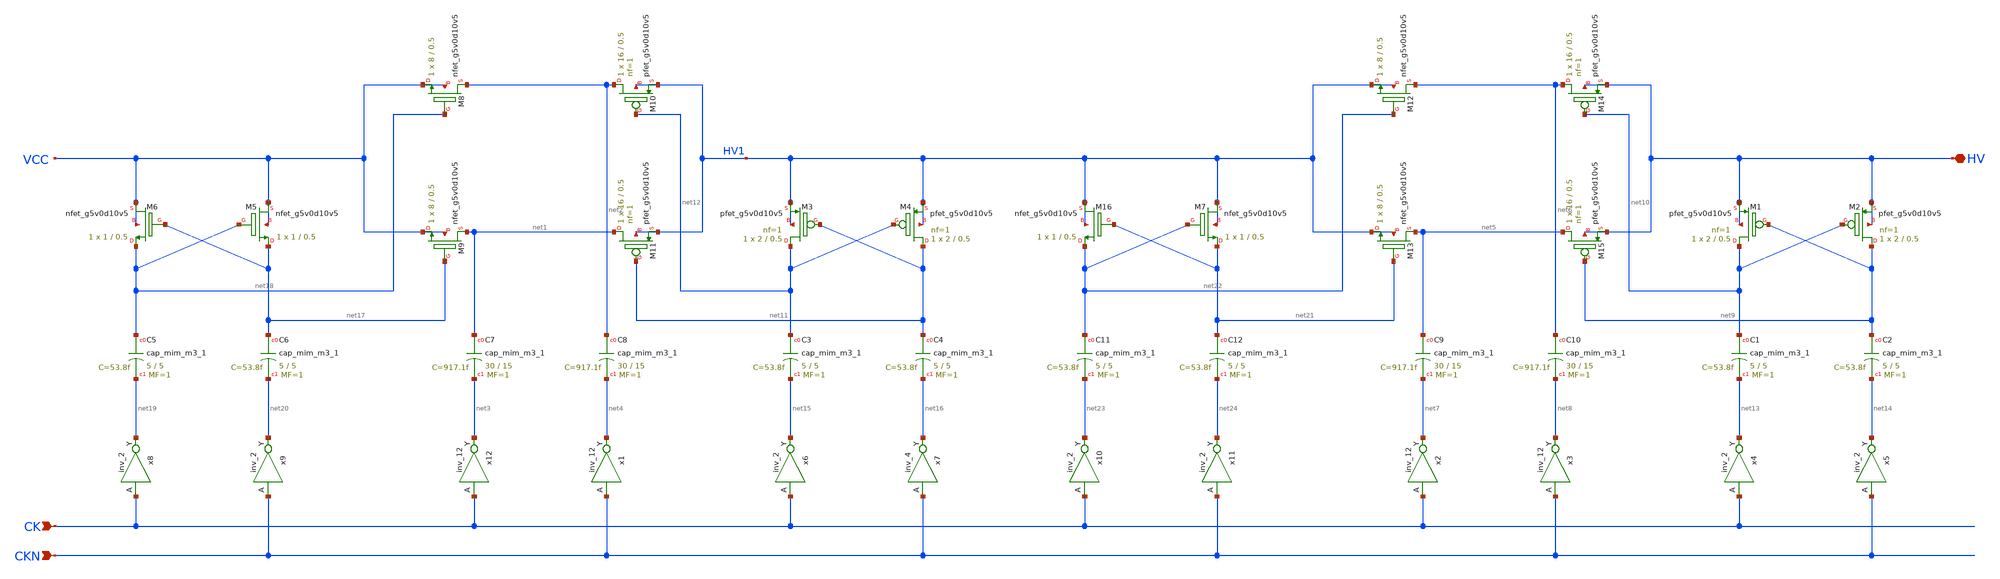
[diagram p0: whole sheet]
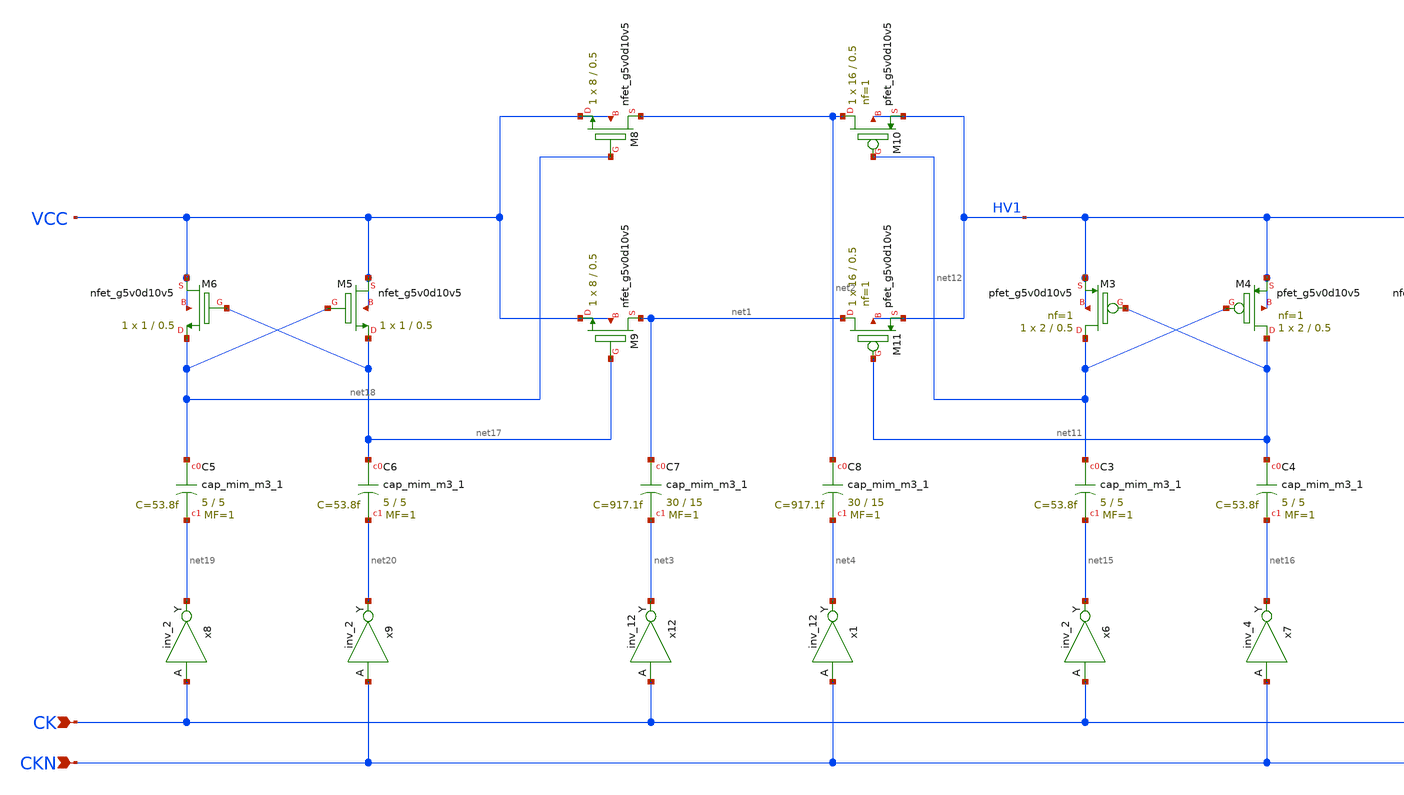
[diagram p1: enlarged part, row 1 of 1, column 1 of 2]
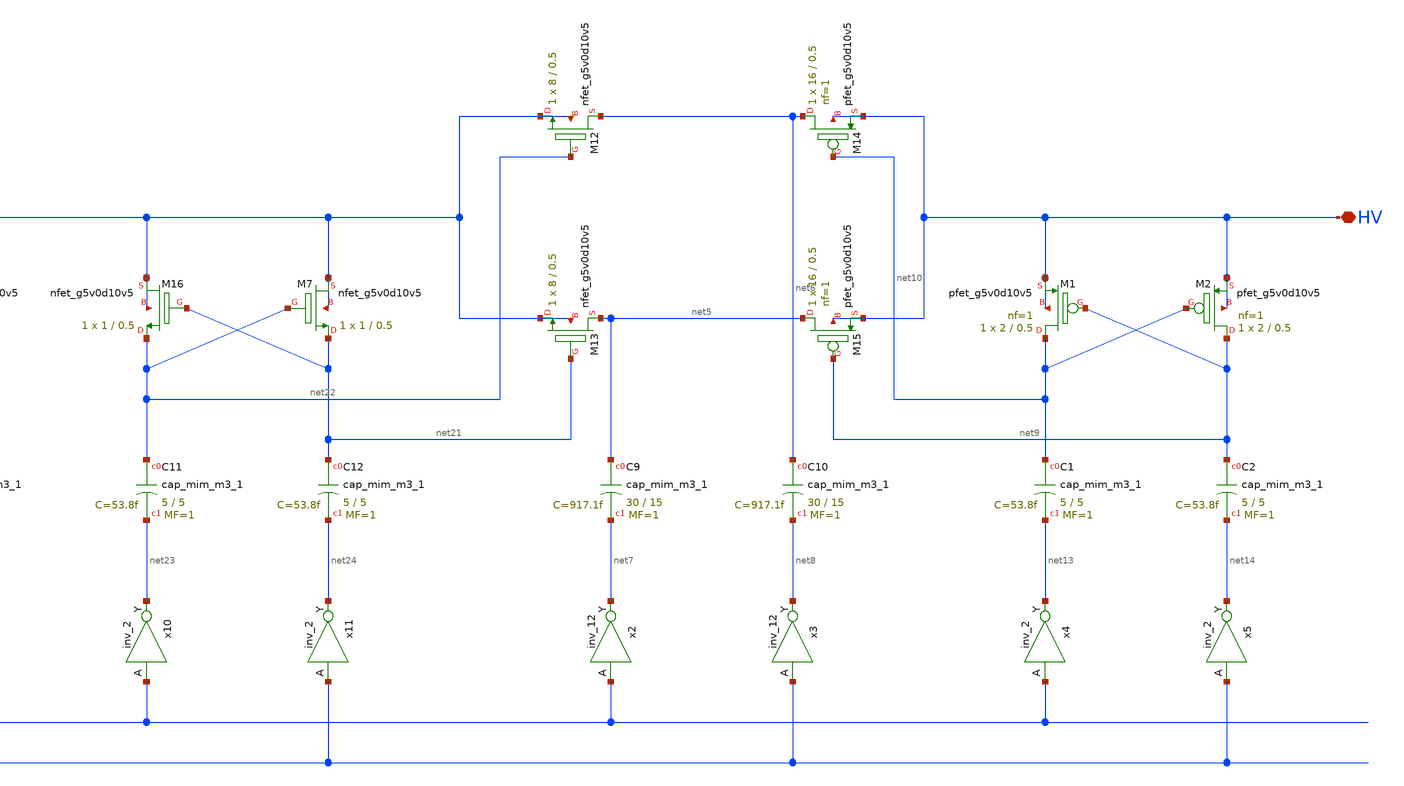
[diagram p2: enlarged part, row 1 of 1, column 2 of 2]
** sch_path: sky130_tests/charge_pump2.sch
**.subckt charge_pump2 HV CK CKN
*.iopin HV
*.ipin CK
*.ipin CKN
XM8 net2 net18 VCC VCC sky130_fd_pr__nfet_g5v0d10v5 W=8 L=0.5 ad='int((nf+1)/2) * W/nf * 0.29' pd='2*int((nf+1)/2) * (W/nf + 0.29)'
+ as='int((nf+2)/2) * W/nf * 0.29' ps='2*int((nf+2)/2) * (W/nf + 0.29)' nrd='0.29 / W' nrs='0.29 / W' sa=0
+ sb=0 sd=0 nf=1 mult=1
XM9 net1 net17 VCC VCC sky130_fd_pr__nfet_g5v0d10v5 W=8 L=0.5 ad='int((nf+1)/2) * W/nf * 0.29' pd='2*int((nf+1)/2) * (W/nf + 0.29)'
+ as='int((nf+2)/2) * W/nf * 0.29' ps='2*int((nf+2)/2) * (W/nf + 0.29)' nrd='0.29 / W' nrs='0.29 / W' sa=0
+ sb=0 sd=0 nf=1 mult=1
XM10 net2 net12 HV1 HV1 sky130_fd_pr__pfet_g5v0d10v5 L=0.5 W=16 nf=1 ad='int((nf+1)/2) * W/nf * 0.29'
+ as='int((nf+2)/2) * W/nf * 0.29' pd='2*int((nf+1)/2) * (W/nf + 0.29)' ps='2*int((nf+2)/2) * (W/nf + 0.29)'
+ nrd='0.29 / W' nrs='0.29 / W' sa=0 sb=0 sd=0 mult=1 m=1
XM11 net1 net11 HV1 HV1 sky130_fd_pr__pfet_g5v0d10v5 L=0.5 W=16 nf=1 ad='int((nf+1)/2) * W/nf * 0.29'
+ as='int((nf+2)/2) * W/nf * 0.29' pd='2*int((nf+1)/2) * (W/nf + 0.29)' ps='2*int((nf+2)/2) * (W/nf + 0.29)'
+ nrd='0.29 / W' nrs='0.29 / W' sa=0 sb=0 sd=0 mult=1 m=1
XC7 net1 net3 sky130_fd_pr__cap_mim_m3_1 W=30 L=15 MF=1 m=1
XC8 net2 net4 sky130_fd_pr__cap_mim_m3_1 W=30 L=15 MF=1 m=1
XM12 net6 net22 HV1 HV1 sky130_fd_pr__nfet_g5v0d10v5 W=8 L=0.5 ad='int((nf+1)/2) * W/nf * 0.29' pd='2*int((nf+1)/2) * (W/nf + 0.29)'
+ as='int((nf+2)/2) * W/nf * 0.29' ps='2*int((nf+2)/2) * (W/nf + 0.29)' nrd='0.29 / W' nrs='0.29 / W' sa=0
+ sb=0 sd=0 nf=1 mult=1
XM13 net5 net21 HV1 HV1 sky130_fd_pr__nfet_g5v0d10v5 W=8 L=0.5 ad='int((nf+1)/2) * W/nf * 0.29' pd='2*int((nf+1)/2) * (W/nf + 0.29)'
+ as='int((nf+2)/2) * W/nf * 0.29' ps='2*int((nf+2)/2) * (W/nf + 0.29)' nrd='0.29 / W' nrs='0.29 / W' sa=0
+ sb=0 sd=0 nf=1 mult=1
XM14 net6 net10 HV HV sky130_fd_pr__pfet_g5v0d10v5 L=0.5 W=16 nf=1 ad='int((nf+1)/2) * W/nf * 0.29' as='int((nf+2)/2) * W/nf * 0.29'
+ pd='2*int((nf+1)/2) * (W/nf + 0.29)' ps='2*int((nf+2)/2) * (W/nf + 0.29)' nrd='0.29 / W' nrs='0.29 / W'
+ sa=0 sb=0 sd=0 mult=1 m=1
XM15 net5 net9 HV HV sky130_fd_pr__pfet_g5v0d10v5 L=0.5 W=16 nf=1 ad='int((nf+1)/2) * W/nf * 0.29' as='int((nf+2)/2) * W/nf * 0.29'
+ pd='2*int((nf+1)/2) * (W/nf + 0.29)' ps='2*int((nf+2)/2) * (W/nf + 0.29)' nrd='0.29 / W' nrs='0.29 / W'
+ sa=0 sb=0 sd=0 mult=1 m=1
XC9 net5 net7 sky130_fd_pr__cap_mim_m3_1 W=30 L=15 MF=1 m=1
XC10 net6 net8 sky130_fd_pr__cap_mim_m3_1 W=30 L=15 MF=1 m=1
x12 CK GND GND VCC VCC net3 sky130_fd_sc_hd__inv_12
x1 CKN GND GND VCC VCC net4 sky130_fd_sc_hd__inv_12
x2 CK GND GND VCC VCC net7 sky130_fd_sc_hd__inv_12
x3 CKN GND GND VCC VCC net8 sky130_fd_sc_hd__inv_12
XM1 net10 net9 HV HV sky130_fd_pr__pfet_g5v0d10v5 L=0.5 W=2 nf=1 ad='int((nf+1)/2) * W/nf * 0.29' as='int((nf+2)/2) * W/nf * 0.29'
+ pd='2*int((nf+1)/2) * (W/nf + 0.29)' ps='2*int((nf+2)/2) * (W/nf + 0.29)' nrd='0.29 / W' nrs='0.29 / W'
+ sa=0 sb=0 sd=0 mult=1 m=1
XM2 net9 net10 HV HV sky130_fd_pr__pfet_g5v0d10v5 L=0.5 W=2 nf=1 ad='int((nf+1)/2) * W/nf * 0.29' as='int((nf+2)/2) * W/nf * 0.29'
+ pd='2*int((nf+1)/2) * (W/nf + 0.29)' ps='2*int((nf+2)/2) * (W/nf + 0.29)' nrd='0.29 / W' nrs='0.29 / W'
+ sa=0 sb=0 sd=0 mult=1 m=1
XC1 net10 net13 sky130_fd_pr__cap_mim_m3_1 W=5 L=5 MF=1 m=1
XC2 net9 net14 sky130_fd_pr__cap_mim_m3_1 W=5 L=5 MF=1 m=1
XM3 net12 net11 HV1 HV1 sky130_fd_pr__pfet_g5v0d10v5 L=0.5 W=2 nf=1 ad='int((nf+1)/2) * W/nf * 0.29'
+ as='int((nf+2)/2) * W/nf * 0.29' pd='2*int((nf+1)/2) * (W/nf + 0.29)' ps='2*int((nf+2)/2) * (W/nf + 0.29)'
+ nrd='0.29 / W' nrs='0.29 / W' sa=0 sb=0 sd=0 mult=1 m=1
XM4 net11 net12 HV1 HV1 sky130_fd_pr__pfet_g5v0d10v5 L=0.5 W=2 nf=1 ad='int((nf+1)/2) * W/nf * 0.29'
+ as='int((nf+2)/2) * W/nf * 0.29' pd='2*int((nf+1)/2) * (W/nf + 0.29)' ps='2*int((nf+2)/2) * (W/nf + 0.29)'
+ nrd='0.29 / W' nrs='0.29 / W' sa=0 sb=0 sd=0 mult=1 m=1
XC3 net12 net15 sky130_fd_pr__cap_mim_m3_1 W=5 L=5 MF=1 m=1
XC4 net11 net16 sky130_fd_pr__cap_mim_m3_1 W=5 L=5 MF=1 m=1
x4 CK GND GND VCC VCC net13 sky130_fd_sc_hd__inv_2
x5 CKN GND GND VCC VCC net14 sky130_fd_sc_hd__inv_2
x6 CK GND GND VCC VCC net15 sky130_fd_sc_hd__inv_2
x7 CKN GND GND VCC VCC net16 sky130_fd_sc_hd__inv_4
XC5 net18 net19 sky130_fd_pr__cap_mim_m3_1 W=5 L=5 MF=1 m=1
XC6 net17 net20 sky130_fd_pr__cap_mim_m3_1 W=5 L=5 MF=1 m=1
x8 CK GND GND VCC VCC net19 sky130_fd_sc_hd__inv_2
x9 CKN GND GND VCC VCC net20 sky130_fd_sc_hd__inv_2
XM5 VCC net18 net17 VCC sky130_fd_pr__nfet_g5v0d10v5 W=1 L=0.5 ad='int((nf+1)/2) * W/nf * 0.29' pd='2*int((nf+1)/2) * (W/nf + 0.29)'
+ as='int((nf+2)/2) * W/nf * 0.29' ps='2*int((nf+2)/2) * (W/nf + 0.29)' nrd='0.29 / W' nrs='0.29 / W' sa=0
+ sb=0 sd=0 nf=1 mult=1
XM6 VCC net17 net18 VCC sky130_fd_pr__nfet_g5v0d10v5 W=1 L=0.5 ad='int((nf+1)/2) * W/nf * 0.29' pd='2*int((nf+1)/2) * (W/nf + 0.29)'
+ as='int((nf+2)/2) * W/nf * 0.29' ps='2*int((nf+2)/2) * (W/nf + 0.29)' nrd='0.29 / W' nrs='0.29 / W' sa=0
+ sb=0 sd=0 nf=1 mult=1
XC11 net22 net23 sky130_fd_pr__cap_mim_m3_1 W=5 L=5 MF=1 m=1
XC12 net21 net24 sky130_fd_pr__cap_mim_m3_1 W=5 L=5 MF=1 m=1
x10 CK GND GND VCC VCC net23 sky130_fd_sc_hd__inv_2
x11 CKN GND GND VCC VCC net24 sky130_fd_sc_hd__inv_2
XM7 HV1 net22 net21 HV1 sky130_fd_pr__nfet_g5v0d10v5 W=1 L=0.5 ad='int((nf+1)/2) * W/nf * 0.29' pd='2*int((nf+1)/2) * (W/nf + 0.29)'
+ as='int((nf+2)/2) * W/nf * 0.29' ps='2*int((nf+2)/2) * (W/nf + 0.29)' nrd='0.29 / W' nrs='0.29 / W' sa=0
+ sb=0 sd=0 nf=1 mult=1
XM16 HV1 net21 net22 HV1 sky130_fd_pr__nfet_g5v0d10v5 W=1 L=0.5 ad='int((nf+1)/2) * W/nf * 0.29' pd='2*int((nf+1)/2) * (W/nf + 0.29)'
+ as='int((nf+2)/2) * W/nf * 0.29' ps='2*int((nf+2)/2) * (W/nf + 0.29)' nrd='0.29 / W' nrs='0.29 / W' sa=0
+ sb=0 sd=0 nf=1 mult=1
**.ends
.end
